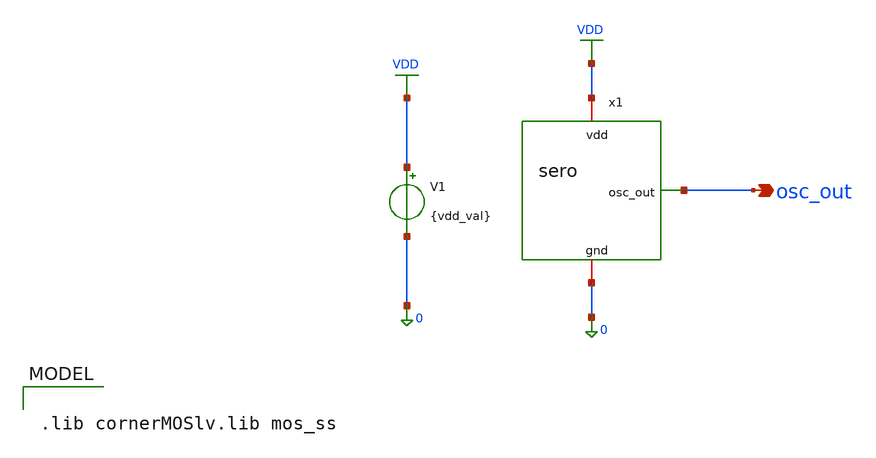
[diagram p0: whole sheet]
** sch_path: simulations/tb/vdd_v_freq.sch
**.subckt vdd_v_freq osc_out
*.opin osc_out
x1 VDD osc_out 0 sero
V1 VDD 0 {vdd_val}
**** begin user architecture code

.lib cornerMOSlv.lib mos_ss



.param length=150n
.param vdd_val=1.2
.param temp=27

.control
  save all
  let v_start = 0.96
  let v_stop  = 1.44
  let v_step  = 0.06
  let n_pts   = 9
  let vdds  = vector(n_pts)
  let freqs = vector(n_pts)
  let powers = vector(n_pts)
  let idx = 0

  while idx < n_pts
    let v_curr = v_start + idx * v_step
    alterparam vdd_val = $&v_curr
    reset
    tran 2p 6n
    meas tran t1 when v(osc_out)=0.5*v_curr rise=4
    meas tran t2 when v(osc_out)=0.5*v_curr rise=5
    meas tran iavg avg i(v1) from=2n to=6n
    let freqs[idx] = 1 / (t2 - t1)
    let powers[idx] = -iavg * v_curr
    let vdds[idx]  = v_curr
    let idx = idx + 1
  end

  set curplot = control
  write vdd_v_freq.raw freqs vdds powers
.endc



**** end user architecture code
**.ends
.GLOBAL VDD
.end
